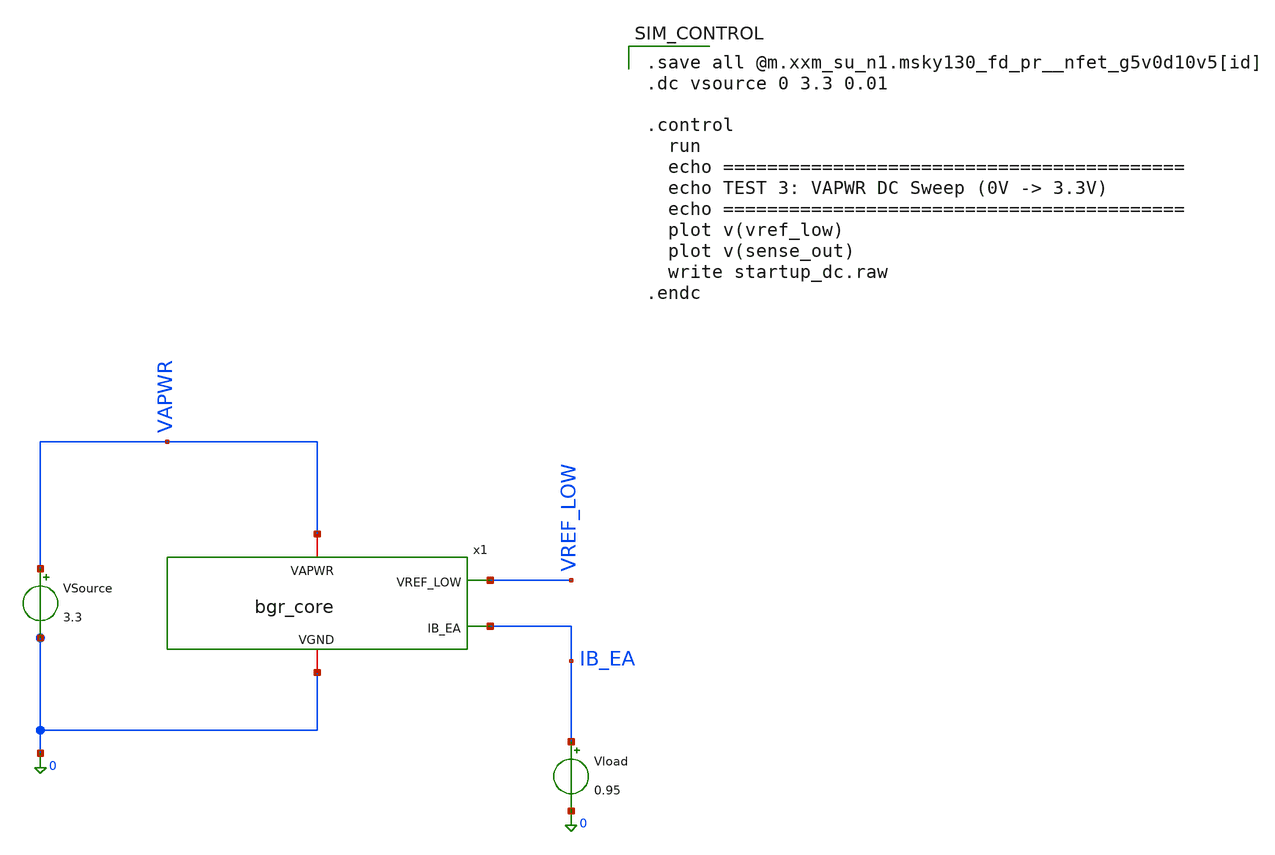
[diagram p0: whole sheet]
** sch_path: designs/bgr_ldo/bgr/bgr_core_tb2.sch
**.subckt bgr_core_tb2
VSource VAPWR 0 3.3
x1 VAPWR VREF_LOW IB_EA 0 bgr_core
Vload IB_EA 0 0.95
**** begin user architecture code

.save all @m.xxm_su_n1.msky130_fd_pr__nfet_g5v0d10v5[id]
.dc vsource 0 3.3 0.01

.control
  run
  echo ==========================================
  echo TEST 3: VAPWR DC Sweep (0V -> 3.3V)
  echo ==========================================
  plot v(vref_low)
  plot v(sense_out)
  write startup_dc.raw
.endc


** opencircuitdesign pdks install
.lib $::SKYWATER_MODELS/sky130.lib.spice tt

**** end user architecture code
**.ends

* expanding   symbol:  bgr_core.sym # of pins=4
** sym_path: designs/bgr_ldo/milestones/10_ibea_tap/bgr_core.sym
** sch_path: designs/bgr_ldo/milestones/10_ibea_tap/bgr_core.sch
.subckt bgr_core VAPWR VREF_LOW IB_EA VGND
*.iopin VAPWR
*.opin VREF_LOW
*.iopin VGND
*.opin IB_EA
XXQA VGND VGND VBE1 sky130_fd_pr__pnp_05v5_W0p68L0p68 m=1
XXQB VGND VGND VBE8 sky130_fd_pr__pnp_05v5_W0p68L0p68 m=8
XXM_top1 net2 V_gate_top VAPWR VAPWR sky130_fd_pr__pfet_g5v0d10v5 L=4 W=20 nf=1 ad='int((1 + 1)/2) * 20 / 1 * 0.29'
+ as='int((1 + 2)/2) * 20 / 1 * 0.29' pd='2*int((1 + 1)/2) * (20 / 1 + 0.29)' ps='2*int((1 + 2)/2) * (20 / 1 + 0.29)'
+ nrd='0.29 / 20 ' nrs='0.29 / 20 ' sa=0 sb=0 sd=0 mult=4 m=4
XXM_top2 net3 V_gate_top VAPWR VAPWR sky130_fd_pr__pfet_g5v0d10v5 L=4 W=20 nf=1 ad='int((1 + 1)/2) * 20 / 1 * 0.29'
+ as='int((1 + 2)/2) * 20 / 1 * 0.29' pd='2*int((1 + 1)/2) * (20 / 1 + 0.29)' ps='2*int((1 + 2)/2) * (20 / 1 + 0.29)'
+ nrd='0.29 / 20 ' nrs='0.29 / 20 ' sa=0 sb=0 sd=0 mult=4 m=4
XXM_top5 net6 V_gate_top VAPWR VAPWR sky130_fd_pr__pfet_g5v0d10v5 L=4 W=20 nf=1 ad='int((1 + 1)/2) * 20 / 1 * 0.29'
+ as='int((1 + 2)/2) * 20 / 1 * 0.29' pd='2*int((1 + 1)/2) * (20 / 1 + 0.29)' ps='2*int((1 + 2)/2) * (20 / 1 + 0.29)'
+ nrd='0.29 / 20 ' nrs='0.29 / 20 ' sa=0 sb=0 sd=0 mult=4 m=4
XXM3 net4 V_mid1 VBE1 VGND sky130_fd_pr__nfet_g5v0d10v5 L=4 W=20 nf=1 ad='int((1 + 1)/2) * 20 / 1 * 0.29'
+ as='int((1 + 2)/2) * 20 / 1 * 0.29' pd='2*int((1 + 1)/2) * (20 / 1 + 0.29)' ps='2*int((1 + 2)/2) * (20 / 1 + 0.29)'
+ nrd='0.29 / 20 ' nrs='0.29 / 20 ' sa=0 sb=0 sd=0 mult=2 m=2
XXM4 net5 V_mid1 net1 VGND sky130_fd_pr__nfet_g5v0d10v5 L=4 W=20 nf=1 ad='int((1 + 1)/2) * 20 / 1 * 0.29'
+ as='int((1 + 2)/2) * 20 / 1 * 0.29' pd='2*int((1 + 1)/2) * (20 / 1 + 0.29)' ps='2*int((1 + 2)/2) * (20 / 1 + 0.29)'
+ nrd='0.29 / 20 ' nrs='0.29 / 20 ' sa=0 sb=0 sd=0 mult=2 m=2
XXM_bot1 V_mid1 V_bias net2 VAPWR sky130_fd_pr__pfet_g5v0d10v5 L=2 W=10 nf=1 ad='int((1 + 1)/2) * 10 / 1 * 0.29'
+ as='int((1 + 2)/2) * 10 / 1 * 0.29' pd='2*int((1 + 1)/2) * (10 / 1 + 0.29)' ps='2*int((1 + 2)/2) * (10 / 1 + 0.29)'
+ nrd='0.29 / 10 ' nrs='0.29 / 10 ' sa=0 sb=0 sd=0 mult=4 m=4
XXM_bot2 V_gate_top V_bias net3 VAPWR sky130_fd_pr__pfet_g5v0d10v5 L=2 W=10 nf=1 ad='int((1 + 1)/2) * 10 / 1 * 0.29'
+ as='int((1 + 2)/2) * 10 / 1 * 0.29' pd='2*int((1 + 1)/2) * (10 / 1 + 0.29)' ps='2*int((1 + 2)/2) * (10 / 1 + 0.29)'
+ nrd='0.29 / 10 ' nrs='0.29 / 10 ' sa=0 sb=0 sd=0 mult=4 m=4
XXM_bot5 VREF_LOW V_bias net6 VAPWR sky130_fd_pr__pfet_g5v0d10v5 L=2 W=10 nf=1 ad='int((1 + 1)/2) * 10 / 1 * 0.29'
+ as='int((1 + 2)/2) * 10 / 1 * 0.29' pd='2*int((1 + 1)/2) * (10 / 1 + 0.29)' ps='2*int((1 + 2)/2) * (10 / 1 + 0.29)'
+ nrd='0.29 / 10 ' nrs='0.29 / 10 ' sa=0 sb=0 sd=0 mult=4 m=4
XXM_bias V_bias V_bias VAPWR VAPWR sky130_fd_pr__pfet_g5v0d10v5 L=4 W=10 nf=1 ad='int((1 + 1)/2) * 10 / 1 * 0.29'
+ as='int((1 + 2)/2) * 10 / 1 * 0.29' pd='2*int((1 + 1)/2) * (10 / 1 + 0.29)' ps='2*int((1 + 2)/2) * (10 / 1 + 0.29)'
+ nrd='0.29 / 10 ' nrs='0.29 / 10 ' sa=0 sb=0 sd=0 mult=1 m=1
XXM_bias_mir V_bias_n V_gate_top VAPWR VAPWR sky130_fd_pr__pfet_g5v0d10v5 L=2 W=10 nf=1 ad='int((1 + 1)/2) * 10 / 1 * 0.29'
+ as='int((1 + 2)/2) * 10 / 1 * 0.29' pd='2*int((1 + 1)/2) * (10 / 1 + 0.29)' ps='2*int((1 + 2)/2) * (10 / 1 + 0.29)'
+ nrd='0.29 / 10 ' nrs='0.29 / 10 ' sa=0 sb=0 sd=0 mult=4 m=4
XXM_bias_n1 V_bias_n V_bias_n VGND VGND sky130_fd_pr__nfet_g5v0d10v5 L=2 W=10 nf=1 ad='int((1 + 1)/2) * 10 / 1 * 0.29'
+ as='int((1 + 2)/2) * 10 / 1 * 0.29' pd='2*int((1 + 1)/2) * (10 / 1 + 0.29)' ps='2*int((1 + 2)/2) * (10 / 1 + 0.29)'
+ nrd='0.29 / 10 ' nrs='0.29 / 10 ' sa=0 sb=0 sd=0 mult=2 m=2
XXM_bias_n2 V_bias V_bias_n VGND VGND sky130_fd_pr__nfet_g5v0d10v5 L=2 W=10 nf=1 ad='int((1 + 1)/2) * 10 / 1 * 0.29'
+ as='int((1 + 2)/2) * 10 / 1 * 0.29' pd='2*int((1 + 1)/2) * (10 / 1 + 0.29)' ps='2*int((1 + 2)/2) * (10 / 1 + 0.29)'
+ nrd='0.29 / 10 ' nrs='0.29 / 10 ' sa=0 sb=0 sd=0 mult=2 m=2
XXM_su_n1 V_gate_top sense_out V_su_mid VGND sky130_fd_pr__nfet_g5v0d10v5 L=2 W=1 nf=1 ad='int((1 + 1)/2) * 1 / 1 * 0.29'
+ as='int((1 + 2)/2) * 1 / 1 * 0.29' pd='2*int((1 + 1)/2) * (1 / 1 + 0.29)' ps='2*int((1 + 2)/2) * (1 / 1 + 0.29)'
+ nrd='0.29 / 1 ' nrs='0.29 / 1 ' sa=0 sb=0 sd=0 mult=1 m=1
XXM_su_n2 V_su_mid V_su_mid VGND VGND sky130_fd_pr__nfet_g5v0d10v5 L=20 W=1 nf=1 ad='int((1 + 1)/2) * 1 / 1 * 0.29'
+ as='int((1 + 2)/2) * 1 / 1 * 0.29' pd='2*int((1 + 1)/2) * (1 / 1 + 0.29)' ps='2*int((1 + 2)/2) * (1 / 1 + 0.29)'
+ nrd='0.29 / 1 ' nrs='0.29 / 1 ' sa=0 sb=0 sd=0 mult=1 m=1
XXM_pd sense_out VBE1 VGND VGND sky130_fd_pr__nfet_g5v0d10v5 L=2 W=12 nf=1 ad='int((1 + 1)/2) * 12 / 1 * 0.29'
+ as='int((1 + 2)/2) * 12 / 1 * 0.29' pd='2*int((1 + 1)/2) * (12 / 1 + 0.29)' ps='2*int((1 + 2)/2) * (12 / 1 + 0.29)'
+ nrd='0.29 / 12 ' nrs='0.29 / 12 ' sa=0 sb=0 sd=0 mult=1 m=1
XXM_su1a sense_out V_bias_n net8 VAPWR sky130_fd_pr__pfet_g5v0d10v5 L=20 W=0.42 nf=1 ad='int((1 + 1)/2) * 0.42 / 1 * 0.29'
+ as='int((1 + 2)/2) * 0.42 / 1 * 0.29' pd='2*int((1 + 1)/2) * (0.42 / 1 + 0.29)' ps='2*int((1 + 2)/2) * (0.42 / 1 + 0.29)'
+ nrd='0.29 / 0.42 ' nrs='0.29 / 0.42 ' sa=0 sb=0 sd=0 mult=1 m=1
XXM_su1b net8 V_bias_n net7 VAPWR sky130_fd_pr__pfet_g5v0d10v5 L=20 W=0.42 nf=1 ad='int((1 + 1)/2) * 0.42 / 1 * 0.29'
+ as='int((1 + 2)/2) * 0.42 / 1 * 0.29' pd='2*int((1 + 1)/2) * (0.42 / 1 + 0.29)' ps='2*int((1 + 2)/2) * (0.42 / 1 + 0.29)'
+ nrd='0.29 / 0.42 ' nrs='0.29 / 0.42 ' sa=0 sb=0 sd=0 mult=1 m=1
XXM_su1c net7 V_bias_n VAPWR VAPWR sky130_fd_pr__pfet_g5v0d10v5 L=20 W=0.42 nf=1 ad='int((1 + 1)/2) * 0.42 / 1 * 0.29'
+ as='int((1 + 2)/2) * 0.42 / 1 * 0.29' pd='2*int((1 + 1)/2) * (0.42 / 1 + 0.29)' ps='2*int((1 + 2)/2) * (0.42 / 1 + 0.29)'
+ nrd='0.29 / 0.42 ' nrs='0.29 / 0.42 ' sa=0 sb=0 sd=0 mult=1 m=1
XR1 VBE8 net1 VGND sky130_fd_pr__res_high_po_0p69 L=34.431 mult=1 m=1
XR6 VGND VBE1 VGND sky130_fd_pr__res_high_po_0p69 L=244.537 mult=1 m=1
XR7 VGND net1 VGND sky130_fd_pr__res_high_po_0p69 L=244.537 mult=1 m=1
XR2 VGND VREF_LOW VGND sky130_fd_pr__res_high_po_0p69 L=244.537 mult=1 m=1
XXM3c V_mid1 V_casc_n net4 VGND sky130_fd_pr__nfet_g5v0d10v5 L=2 W=10 nf=1 ad='int((1 + 1)/2) * 10 / 1 * 0.29'
+ as='int((1 + 2)/2) * 10 / 1 * 0.29' pd='2*int((1 + 1)/2) * (10 / 1 + 0.29)' ps='2*int((1 + 2)/2) * (10 / 1 + 0.29)'
+ nrd='0.29 / 10 ' nrs='0.29 / 10 ' sa=0 sb=0 sd=0 mult=2 m=2
XXM4c V_gate_top V_casc_n net5 VGND sky130_fd_pr__nfet_g5v0d10v5 L=2 W=10 nf=1 ad='int((1 + 1)/2) * 10 / 1 * 0.29'
+ as='int((1 + 2)/2) * 10 / 1 * 0.29' pd='2*int((1 + 1)/2) * (10 / 1 + 0.29)' ps='2*int((1 + 2)/2) * (10 / 1 + 0.29)'
+ nrd='0.29 / 10 ' nrs='0.29 / 10 ' sa=0 sb=0 sd=0 mult=2 m=2
XXM_cn_mir V_casc_n V_gate_top VAPWR VAPWR sky130_fd_pr__pfet_g5v0d10v5 L=2 W=10 nf=1 ad='int((1 + 1)/2) * 10 / 1 * 0.29'
+ as='int((1 + 2)/2) * 10 / 1 * 0.29' pd='2*int((1 + 1)/2) * (10 / 1 + 0.29)' ps='2*int((1 + 2)/2) * (10 / 1 + 0.29)'
+ nrd='0.29 / 10 ' nrs='0.29 / 10 ' sa=0 sb=0 sd=0 mult=1 m=1
XXM_cn_d2 V_casc_n V_casc_n cn_mid VGND sky130_fd_pr__nfet_g5v0d10v5 L=2 W=2 nf=1 ad='int((1 + 1)/2) * 2 / 1 * 0.29'
+ as='int((1 + 2)/2) * 2 / 1 * 0.29' pd='2*int((1 + 1)/2) * (2 / 1 + 0.29)' ps='2*int((1 + 2)/2) * (2 / 1 + 0.29)'
+ nrd='0.29 / 2 ' nrs='0.29 / 2 ' sa=0 sb=0 sd=0 mult=1 m=1
XXM_cn_d1 cn_mid cn_mid net9 VGND sky130_fd_pr__nfet_g5v0d10v5 L=2 W=2 nf=1 ad='int((1 + 1)/2) * 2 / 1 * 0.29'
+ as='int((1 + 2)/2) * 2 / 1 * 0.29' pd='2*int((1 + 1)/2) * (2 / 1 + 0.29)' ps='2*int((1 + 2)/2) * (2 / 1 + 0.29)'
+ nrd='0.29 / 2 ' nrs='0.29 / 2 ' sa=0 sb=0 sd=0 mult=1 m=1
XR_cn VGND net9 VGND sky130_fd_pr__res_high_po_0p69 L=91.5 mult=1 m=1
XXM_tap_top net_tap V_gate_top VAPWR VAPWR sky130_fd_pr__pfet_g5v0d10v5 L=4 W=20 nf=1 ad='int((1 + 1)/2) * 20 / 1 * 0.29'
+ as='int((1 + 2)/2) * 20 / 1 * 0.29' pd='2*int((1 + 1)/2) * (20 / 1 + 0.29)' ps='2*int((1 + 2)/2) * (20 / 1 + 0.29)'
+ nrd='0.29 / 20 ' nrs='0.29 / 20 ' sa=0 sb=0 sd=0 mult=1 m=1
XXM_tap_casc IB_EA V_bias net_tap VAPWR sky130_fd_pr__pfet_g5v0d10v5 L=2 W=10 nf=1 ad='int((1 + 1)/2) * 10 / 1 * 0.29'
+ as='int((1 + 2)/2) * 10 / 1 * 0.29' pd='2*int((1 + 1)/2) * (10 / 1 + 0.29)' ps='2*int((1 + 2)/2) * (10 / 1 + 0.29)'
+ nrd='0.29 / 10 ' nrs='0.29 / 10 ' sa=0 sb=0 sd=0 mult=1 m=1
.ends

.end
